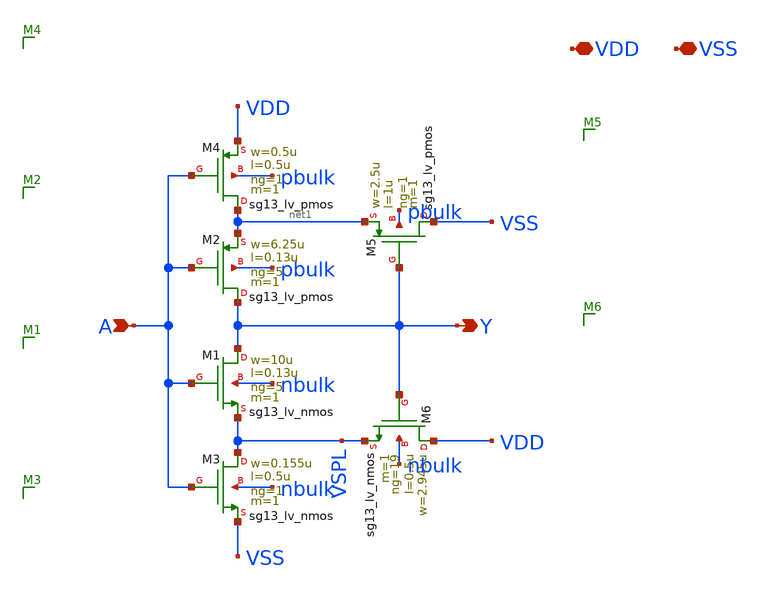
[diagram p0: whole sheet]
** sch_path: dependencies/CLK/CLK-main/schematic/xschem/ring_schmitt.sch
**.subckt ring_schmitt A Y VDD VSS
*.ipin A
*.opin Y
*.iopin VDD
*.iopin VSS
XM1 Y A VSPL nbulk sg13_lv_nmos w=10u l=0.13u ng=5 m=1 mm_ok=1
XM2 Y A net1 pbulk sg13_lv_pmos w=6.25u l=0.13u ng=5 m=1 mm_ok=1
XM3 VSPL A VSS nbulk sg13_lv_nmos w=0.155u l=0.5u ng=1 m=1 mm_ok=1
XM4 net1 A VDD pbulk sg13_lv_pmos w=0.5u l=0.5u ng=1 m=1 mm_ok=1
XM5 VSS Y net1 pbulk sg13_lv_pmos w=2.5u l=1u ng=1 m=1 mm_ok=1
XM6 VDD Y VSPL nbulk sg13_lv_nmos w=2.945u l=0.5u ng=19 m=1 mm_ok=1
**.ends
.end
